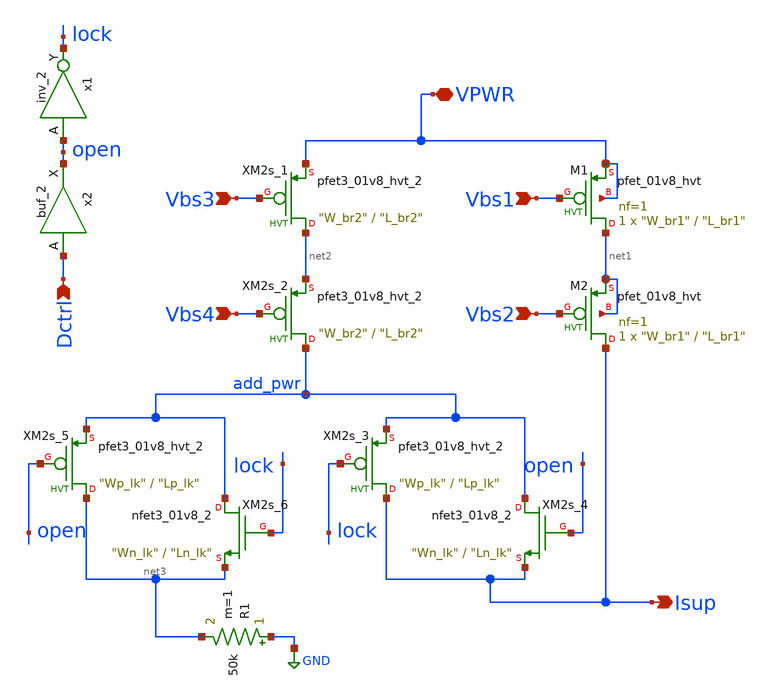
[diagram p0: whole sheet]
** sch_path: xschem/lib/ALib_IDAC.sch
* xschem/lib/nfet3_01v8_2.sym:
* Copyright 2020 Stefan Frederik Schippers
* Licensed under the Apache License, Version 2.0 (the "License");
**.subckt ALib_IDAC Vbs3 Vbs4 Vbs1 Vbs2 VPWR Isup Dctrl
*.ipin Vbs3
*.ipin Vbs4
*.ipin Vbs1
*.ipin Vbs2
*.iopin VPWR
*.opin Isup
*.ipin Dctrl
XM2s_1 net2 Vbs3 VPWR pfet3_01v8_hvt_2 L="L_br2" W="W_br2"
XM2s_2 add_pwr Vbs4 net2 pfet3_01v8_hvt_2 L="L_br2" W="W_br2"
XM2s_3 Isup lock add_pwr pfet3_01v8_hvt_2 L="Lp_lk" W="Wp_lk"
XM2s_4 add_pwr open Isup nfet3_01v8_2 L="Ln_lk" W="Wn_lk"
R1 GND net3 50k m=1
x1 open GND GND VPWR VPWR lock sky130_fd_sc_hd__inv_2
XM1 net1 Vbs1 VPWR VPWR sky130_fd_pr__pfet_01v8_hvt L="L_br1" W="W_br1" nf=1 ad='int((nf+1)/2) * W/nf * 0.29'
+ as='int((nf+2)/2) * W/nf * 0.29' pd='2*int((nf+1)/2) * (W/nf + 0.29)' ps='2*int((nf+2)/2) * (W/nf + 0.29)'
+ nrd='0.29 / W' nrs='0.29 / W' sa=0 sb=0 sd=0 mult=1 m=1
XM2 Isup Vbs2 net1 net1 sky130_fd_pr__pfet_01v8_hvt L="L_br1" W="W_br1" nf=1 ad='int((nf+1)/2) * W/nf * 0.29'
+ as='int((nf+2)/2) * W/nf * 0.29' pd='2*int((nf+1)/2) * (W/nf + 0.29)' ps='2*int((nf+2)/2) * (W/nf + 0.29)'
+ nrd='0.29 / W' nrs='0.29 / W' sa=0 sb=0 sd=0 mult=1 m=1
XM2s_5 net3 open add_pwr pfet3_01v8_hvt_2 L="Lp_lk" W="Wp_lk"
XM2s_6 add_pwr lock net3 nfet3_01v8_2 L="Ln_lk" W="Wn_lk"
x2 Dctrl GND GND VPWR VPWR open sky130_fd_sc_hd__buf_2
**.ends

* expanding   symbol:  pfet3_01v8_hvt_2.sym # of pins=3
** sym_path: xschem/lib/pfet3_01v8_hvt_2.sym
** sch_path: xschem/lib/pfet3_01v8_hvt_2.sch
.subckt pfet3_01v8_hvt_2 D G S  L=0.15 W=1
*.ipin G
*.iopin D
*.iopin S
XM1 S G D S sky130_fd_pr__pfet_01v8_hvt L="L" W="W" nf=1 ad='int((nf+1)/2) * W/nf * 0.29' as='int((nf+2)/2) * W/nf * 0.29'
+ pd='2*int((nf+1)/2) * (W/nf + 0.29)' ps='2*int((nf+2)/2) * (W/nf + 0.29)' nrd='0.29 / W' nrs='0.29 / W'
+ sa=0 sb=0 sd=0 mult=1 m=1
XM2 D G S S sky130_fd_pr__pfet_01v8_hvt L="L" W="W" nf=1 ad='int((nf+1)/2) * W/nf * 0.29' as='int((nf+2)/2) * W/nf * 0.29'
+ pd='2*int((nf+1)/2) * (W/nf + 0.29)' ps='2*int((nf+2)/2) * (W/nf + 0.29)' nrd='0.29 / W' nrs='0.29 / W'
+ sa=0 sb=0 sd=0 mult=1 m=1
.ends


* expanding   symbol:  nfet3_01v8_2.sym # of pins=3
** sym_path: xschem/lib/nfet3_01v8_2.sym
** sch_path: xschem/lib/nfet3_01v8_2.sch
.subckt nfet3_01v8_2 D G S  L=0.15 W=1
*.iopin D
*.iopin G
*.iopin S
XM9 S G D S sky130_fd_pr__nfet_01v8 L="L" W="W" nf=1 ad='int((nf+1)/2) * W/nf * 0.29' as='int((nf+2)/2) * W/nf * 0.29'
+ pd='2*int((nf+1)/2) * (W/nf + 0.29)' ps='2*int((nf+2)/2) * (W/nf + 0.29)' nrd='0.29 / W' nrs='0.29 / W'
+ sa=0 sb=0 sd=0 mult=1 m=1
XM10 D G S S sky130_fd_pr__nfet_01v8 L="L" W="W" nf=1 ad='int((nf+1)/2) * W/nf * 0.29' as='int((nf+2)/2) * W/nf * 0.29'
+ pd='2*int((nf+1)/2) * (W/nf + 0.29)' ps='2*int((nf+2)/2) * (W/nf + 0.29)' nrd='0.29 / W' nrs='0.29 / W'
+ sa=0 sb=0 sd=0 mult=1 m=1
.ends

.GLOBAL GND
.end
